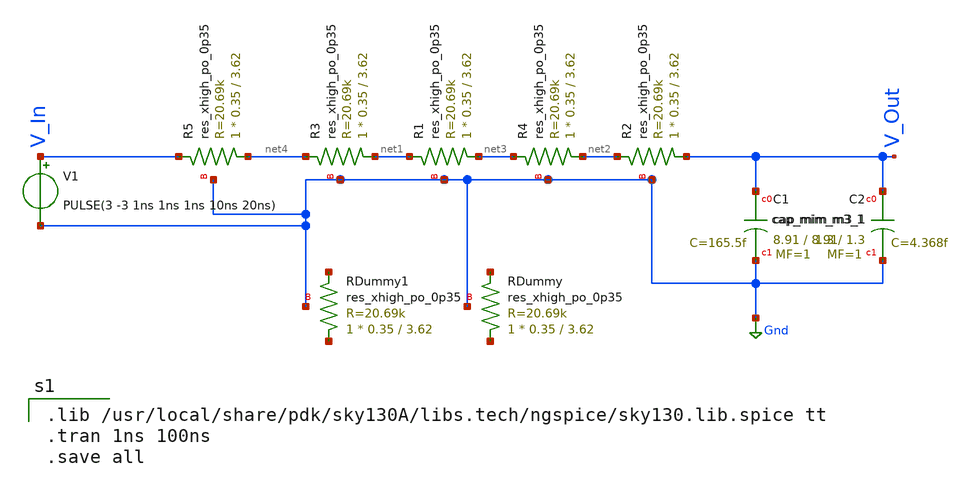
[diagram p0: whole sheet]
** sch_path: Schematic/RC-lowPassFilter/RC-LowPassFilter.sch
**.subckt RC-LowPassFilter
XR3 net1 net4 Gnd sky130_fd_pr__res_xhigh_po_0p35 L=3.62 mult=1 m=1
XR4 net2 net3 Gnd sky130_fd_pr__res_xhigh_po_0p35 L=3.62 mult=1 m=1
XC1 V_Out Gnd sky130_fd_pr__cap_mim_m3_1 W=8.91 L=8.91 MF=1 m=1
XRDummy1 net5 net6 Gnd sky130_fd_pr__res_xhigh_po_0p35 L=3.62 mult=1 m=1
XRDummy net7 net8 Gnd sky130_fd_pr__res_xhigh_po_0p35 L=3.62 mult=1 m=1
XR5 net4 V_In Gnd sky130_fd_pr__res_xhigh_po_0p35 L=3.62 mult=1 m=1
XR1 net3 net1 Gnd sky130_fd_pr__res_xhigh_po_0p35 L=3.62 mult=1 m=1
XR2 V_Out net2 Gnd sky130_fd_pr__res_xhigh_po_0p35 L=3.62 mult=1 m=1
V1 V_In Gnd PULSE(3 -3 1ns 1ns 1ns 10ns 20ns)
XC2 V_Out Gnd sky130_fd_pr__cap_mim_m3_1 W=1.3 L=1.3 MF=1 m=1
**** begin user architecture code

.lib /usr/local/share/pdk/sky130A/libs.tech/ngspice/sky130.lib.spice tt
.tran 1ns 100ns
.save all



**** end user architecture code
**.ends
.GLOBAL Gnd
.end
